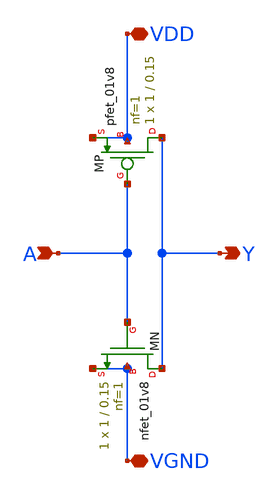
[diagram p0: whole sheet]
** sch_path: src/reversible_stdcells/rev_not/rev_not.sch
**.subckt rev_not VDD VGND A Y
*.iopin VDD
*.iopin VGND
*.ipin A
*.opin Y
XMP Y A VDD VDD sky130_fd_pr__pfet_01v8 L=0.15 W=1 nf=1 ad='int((1 + 1)/2) * 1 / 1 * 0.29' as='int((1 + 2)/2) * 1 / 1 * 0.29'
+ pd='2*int((1 + 1)/2) * (1 / 1 + 0.29)' ps='2*int((1 + 2)/2) * (1 / 1 + 0.29)' nrd='0.29 / 1 ' nrs='0.29 / 1 '
+ sa=0 sb=0 sd=0 mult=1 m=1
XMN Y A VGND VGND sky130_fd_pr__nfet_01v8 L=0.15 W=1 nf=1 ad='int((1 + 1)/2) * 1 / 1 * 0.29' as='int((1 + 2)/2) * 1 / 1 * 0.29'
+ pd='2*int((1 + 1)/2) * (1 / 1 + 0.29)' ps='2*int((1 + 2)/2) * (1 / 1 + 0.29)' nrd='0.29 / 1 ' nrs='0.29 / 1 '
+ sa=0 sb=0 sd=0 mult=1 m=1
**.ends
.end
